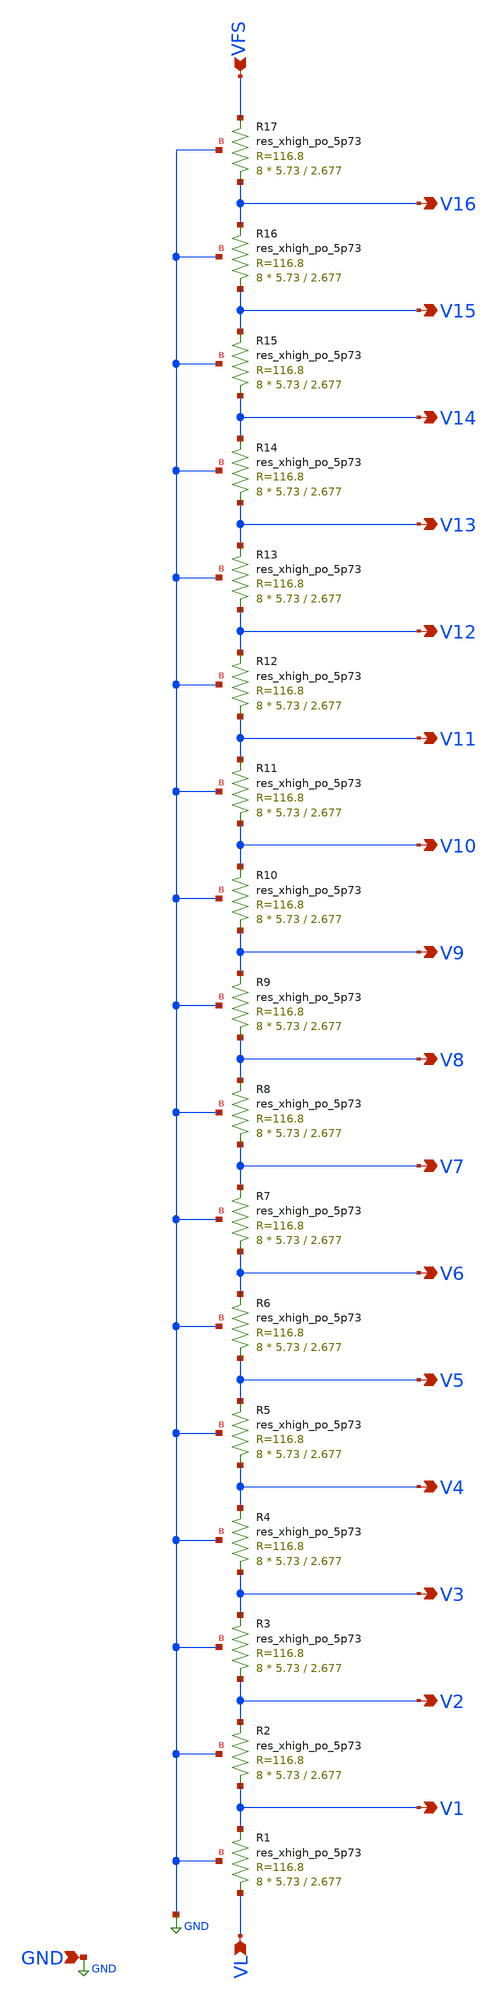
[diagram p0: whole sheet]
** sch_path: flashADC/xschem/resistorDivider_v0p0p1.sch
.lib $::SKYWATER_MODELS/sky130.lib.spice tt
.include $::SKYWATER_STDCELLS/sky130_fd_sc_hd.spice

**.subckt resistorDivider_v0p0p1 VFS V1 V2 V3 V4 V5 V6 V7 V8 V9 V10 V11 V12 V13 V14 V15 V16 VL GND
*.ipin VFS
*.opin V1
*.opin V2
*.opin V3
*.opin V4
*.opin V5
*.opin V6
*.opin V7
*.opin V8
*.opin V9
*.opin V10
*.opin V11
*.opin V12
*.opin V13
*.opin V14
*.opin V15
*.opin V16
*.ipin VL
*.ipin GND
XR1 VL V1 GND sky130_fd_pr__res_xhigh_po_5p73 L=2.677 mult=8 m=8
XR2 V1 V2 GND sky130_fd_pr__res_xhigh_po_5p73 L=2.677 mult=8 m=8
XR3 V2 V3 GND sky130_fd_pr__res_xhigh_po_5p73 L=2.677 mult=8 m=8
XR4 V3 V4 GND sky130_fd_pr__res_xhigh_po_5p73 L=2.677 mult=8 m=8
XR5 V4 V5 GND sky130_fd_pr__res_xhigh_po_5p73 L=2.677 mult=8 m=8
XR6 V5 V6 GND sky130_fd_pr__res_xhigh_po_5p73 L=2.677 mult=8 m=8
XR7 V6 V7 GND sky130_fd_pr__res_xhigh_po_5p73 L=2.677 mult=8 m=8
XR8 V7 V8 GND sky130_fd_pr__res_xhigh_po_5p73 L=2.677 mult=8 m=8
XR9 V8 V9 GND sky130_fd_pr__res_xhigh_po_5p73 L=2.677 mult=8 m=8
XR10 V9 V10 GND sky130_fd_pr__res_xhigh_po_5p73 L=2.677 mult=8 m=8
XR11 V10 V11 GND sky130_fd_pr__res_xhigh_po_5p73 L=2.677 mult=8 m=8
XR12 V11 V12 GND sky130_fd_pr__res_xhigh_po_5p73 L=2.677 mult=8 m=8
XR13 V12 V13 GND sky130_fd_pr__res_xhigh_po_5p73 L=2.677 mult=8 m=8
XR14 V13 V14 GND sky130_fd_pr__res_xhigh_po_5p73 L=2.677 mult=8 m=8
XR15 V14 V15 GND sky130_fd_pr__res_xhigh_po_5p73 L=2.677 mult=8 m=8
XR16 V15 V16 GND sky130_fd_pr__res_xhigh_po_5p73 L=2.677 mult=8 m=8
XR17 V16 VFS GND sky130_fd_pr__res_xhigh_po_5p73 L=2.677 mult=8 m=8
**.ends
.GLOBAL GND
.end
